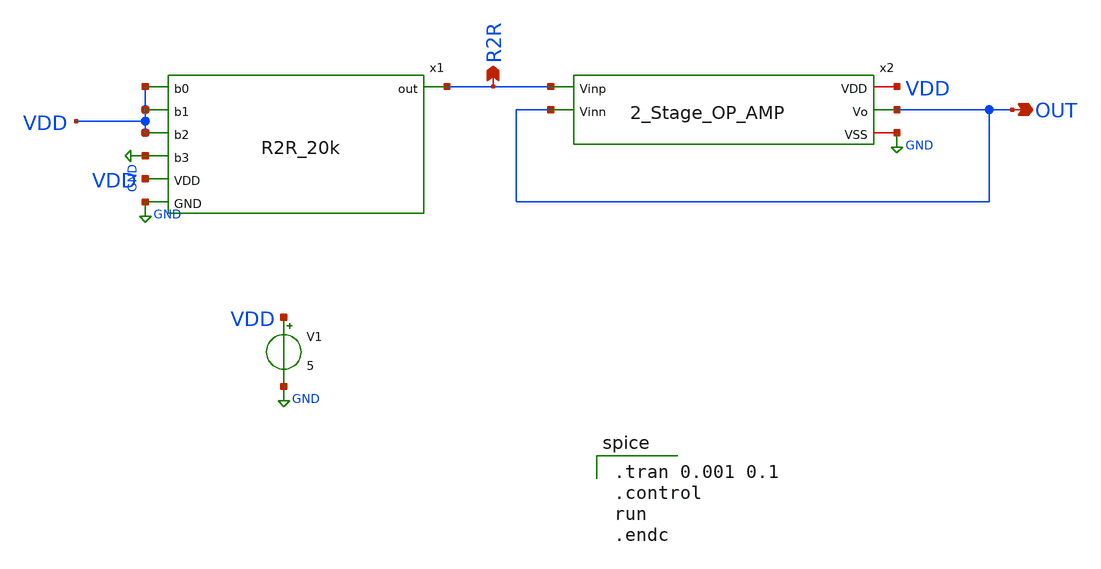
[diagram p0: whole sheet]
** sch_path: ADC/4bit_C2C/MagicAndSpice/EE431_FinalProj/DAC.sch
**.subckt DAC OUT R2R
*.opin OUT
*.opin R2R
V1 VDD GND 5
x2 VDD R2R OUT OUT GND 2_Stage_OP_AMP
x1 R2R VDD VDD GND VDD VDD GND R2R_20k
**** begin user architecture code
 .lib $::SKYWATER_MODELS/sky130.lib.spice tt

.tran 0.001 0.1
.control
run
.endc

**** end user architecture code
**.ends
.GLOBAL GND
.end
